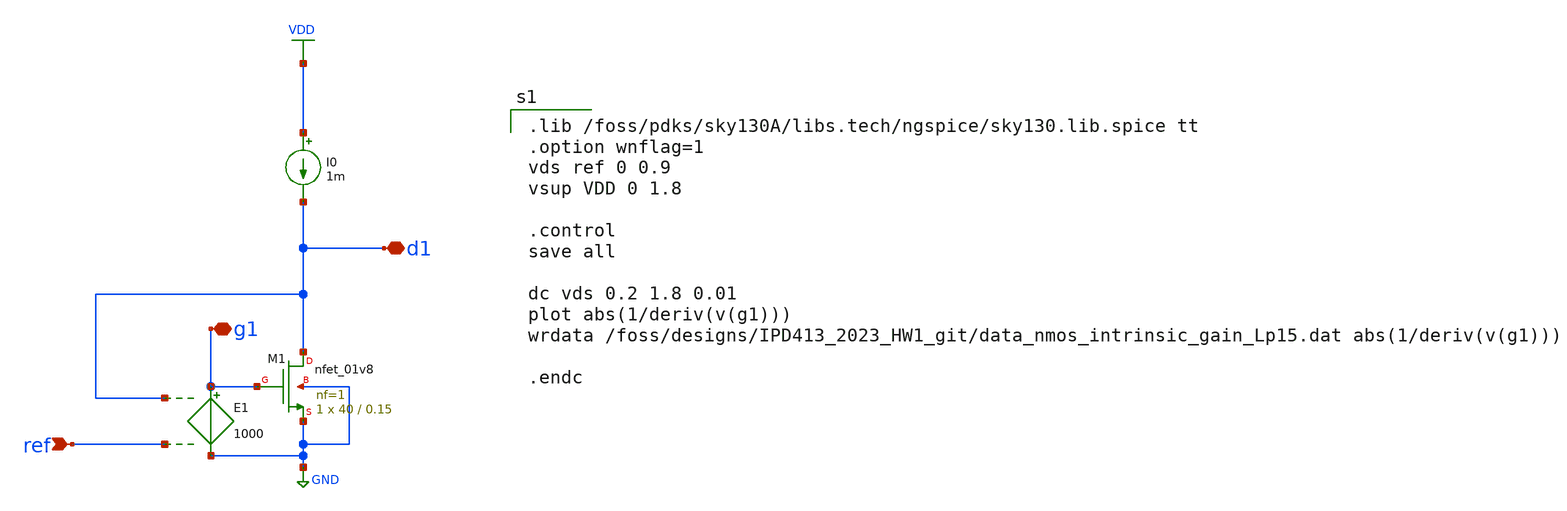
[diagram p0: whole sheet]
** sch_path: nmos_intrinsic_gain_IPD413HW1.sch
**.subckt nmos_intrinsic_gain_IPD413HW1 ref g1 d1
*.ipin ref
*.iopin g1
*.iopin d1
E1 g1 GND d1 ref 1000
I0 VDD d1 1m
XM1 d1 g1 GND GND sky130_fd_pr__nfet_01v8 L=0.15 W=40 nf=1 ad='int((nf+1)/2) * W/nf * 0.29' as='int((nf+2)/2) * W/nf * 0.29'
+ pd='2*int((nf+1)/2) * (W/nf + 0.29)' ps='2*int((nf+2)/2) * (W/nf + 0.29)' nrd='0.29 / W' nrs='0.29 / W'
+ sa=0 sb=0 sd=0 mult=1 m=1
**** begin user architecture code

.lib /foss/pdks/sky130A/libs.tech/ngspice/sky130.lib.spice tt
.option wnflag=1
vds ref 0 0.9
vsup VDD 0 1.8

.control
save all

dc vds 0.2 1.8 0.01
plot abs(1/deriv(v(g1)))
wrdata /foss/designs/IPD413_2023_HW1_git/data_nmos_intrinsic_gain_Lp15.dat abs(1/deriv(v(g1)))

.endc

**** end user architecture code
**.ends
.GLOBAL GND
.GLOBAL VDD
.end
